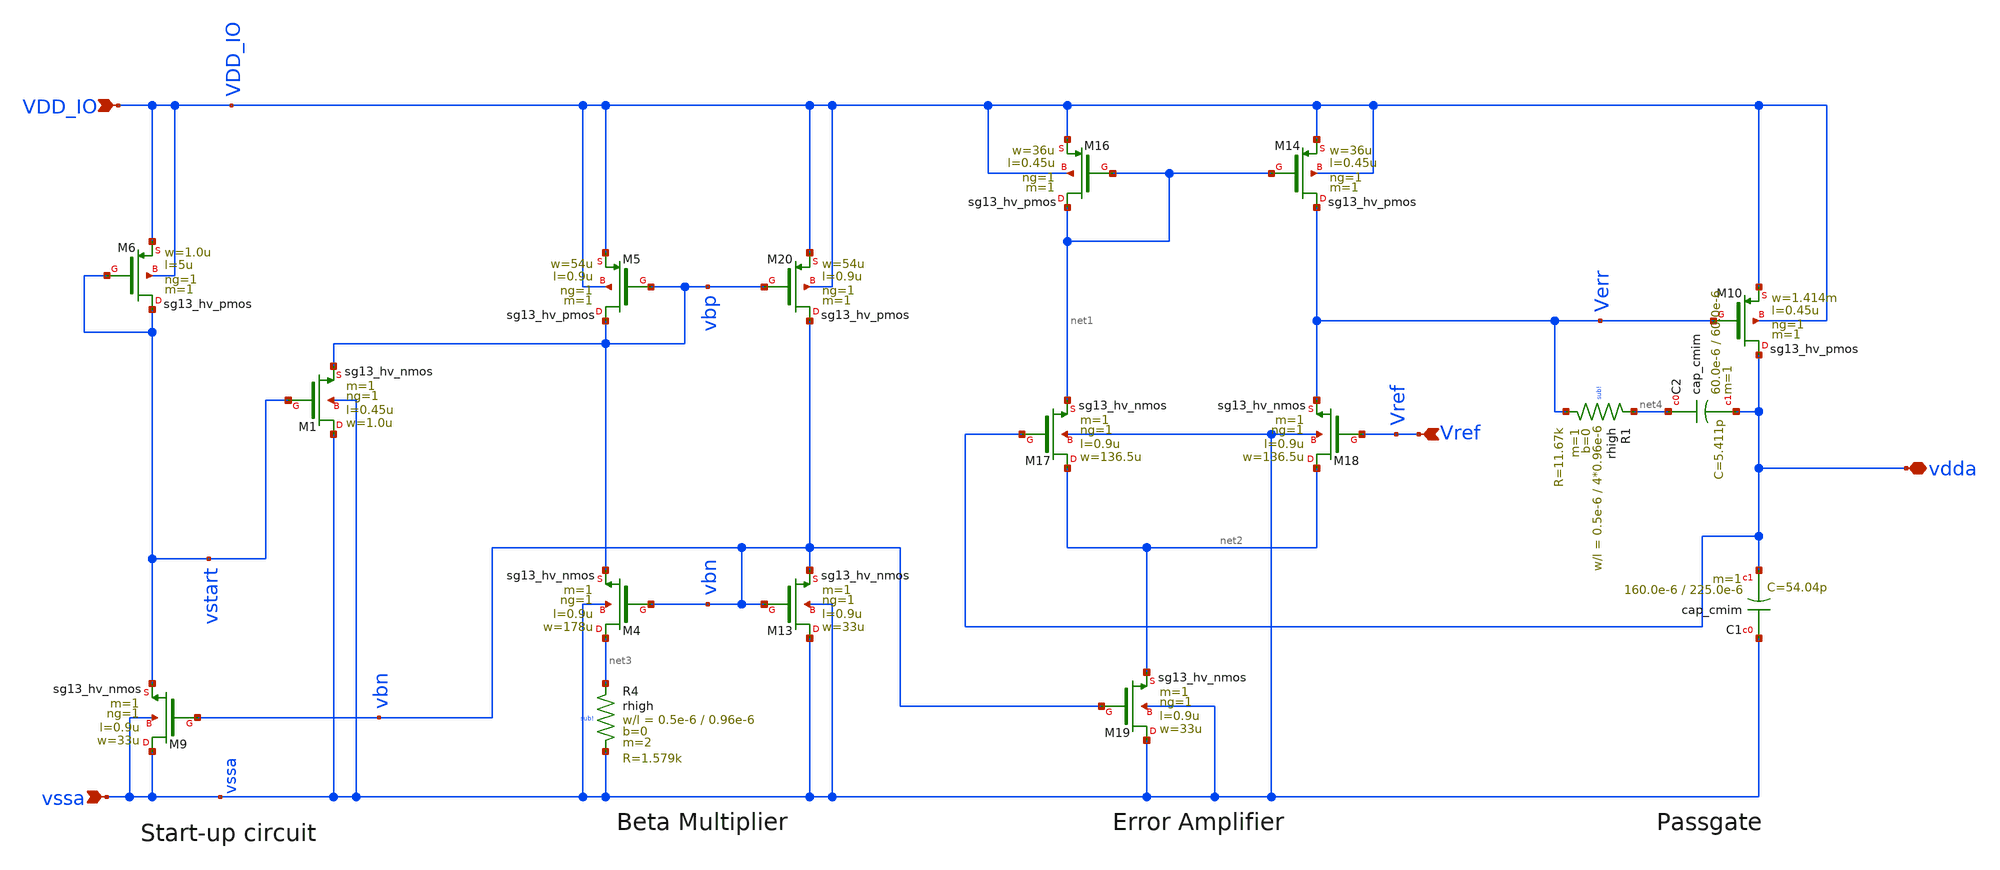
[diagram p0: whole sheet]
** sch_path: 5_Design/4_Layout/Team 2 - Transformer Monster Tractors/xschem/LDO_TOP_T2.sch
**.subckt LDO_TOP_T2 VDD_IO vssa Vref vdda
*.ipin VDD_IO
*.ipin vssa
*.ipin Vref
*.iopin vdda
XM14 Verr net1 VDD_IO VDD_IO sg13_hv_pmos w=36u l=0.45u ng=1 m=1 mm_ok=1
XM16 net1 net1 VDD_IO VDD_IO sg13_hv_pmos w=36u l=0.45u ng=1 m=1 mm_ok=1
XM17 net2 vdda net1 vssa sg13_hv_nmos w=136.5u l=0.9u ng=1 m=1 mm_ok=1
XM18 net2 Vref Verr vssa sg13_hv_nmos w=136.5u l=0.9u ng=1 m=1 mm_ok=1
XM19 vssa vbn net2 vssa sg13_hv_nmos w=33u l=0.9u ng=1 m=1 mm_ok=1
XM6 vstart vstart VDD_IO VDD_IO sg13_hv_pmos w=1.0u l=5u ng=1 m=1 mm_ok=1
XM1 vssa vstart vbp vssa sg13_hv_nmos w=1.0u l=0.45u ng=1 m=1 mm_ok=1
XM9 vssa vbn vstart vssa sg13_hv_nmos w=33u l=0.9u ng=1 m=1 mm_ok=1
XM4 net3 vbn vbp vssa sg13_hv_nmos w=178u l=0.9u ng=1 m=1 mm_ok=1
XM13 vssa vbn vbn vssa sg13_hv_nmos w=33u l=0.9u ng=1 m=1 mm_ok=1
XM5 vbp vbp VDD_IO VDD_IO sg13_hv_pmos w=54u l=0.9u ng=1 m=1 mm_ok=1
XM20 vbn vbp VDD_IO VDD_IO sg13_hv_pmos w=54u l=0.9u ng=1 m=1 mm_ok=1
XR4 net3 vssa sub! rhigh w=0.5e-6 l=0.96e-6 m=2 b=0 mm_ok=1
XC1 vssa vdda cap_cmim w=160.0e-6 l=225.0e-6 m=1 mm_ok=1
XM10 vdda Verr VDD_IO VDD_IO sg13_hv_pmos w=1.414m l=0.45u ng=1 m=1 mm_ok=1
XC2 net4 vdda cap_cmim w=60.0e-6 l=60.0e-6 m=1 mm_ok=1
XR1 net4 Verr sub! rhigh w=0.5e-6 l=4*0.96e-6 m=1 b=0 mm_ok=1
**.ends
.end
